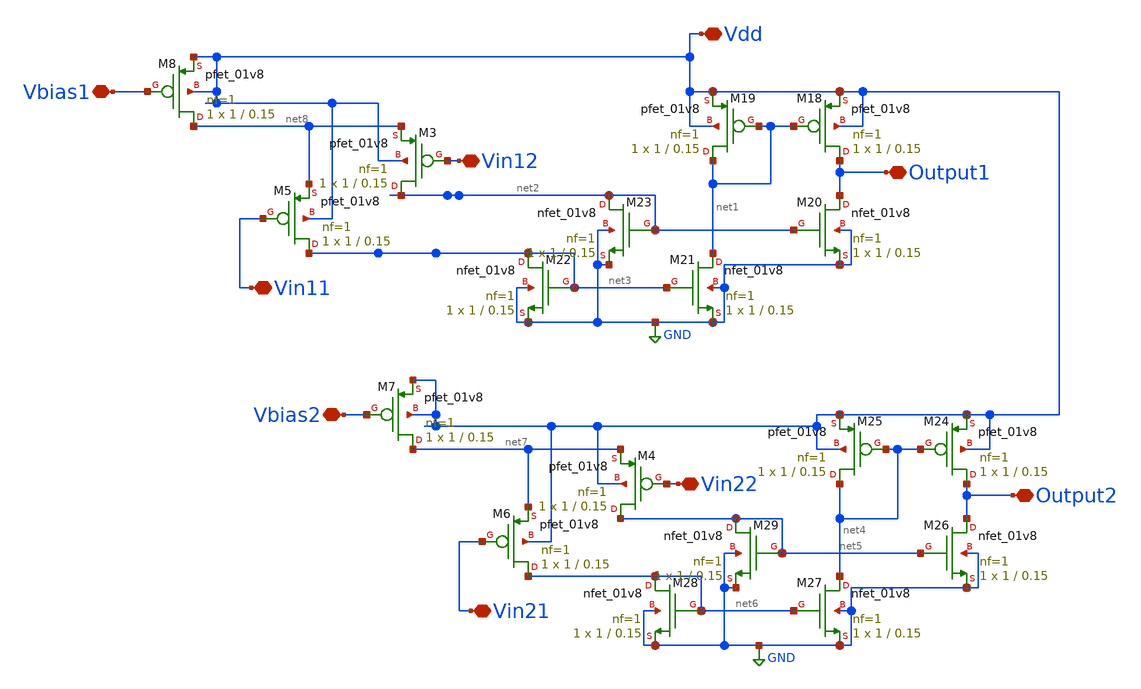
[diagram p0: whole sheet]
** sch_path: libs.ref/sky130_hilas_sc/xschem/TA2SignalBiasCell.sch
**.subckt TA2SignalBiasCell Vdd Output1 Output2 Vin21 Vin22 Vin11 Vin12 Vbias1 Vbias2
*.iopin Vdd
*.iopin Output1
*.iopin Output2
*.iopin Vin21
*.iopin Vin22
*.iopin Vin11
*.iopin Vin12
*.iopin Vbias1
*.iopin Vbias2
XM18 Output1 net1 Vdd Vdd sky130_fd_pr__pfet_01v8 L=0.15 W=1 nf=1 ad='int((nf+1)/2) * W/nf * 0.29' as='int((nf+2)/2) * W/nf * 0.29'
+ pd='2*int((nf+1)/2) * (W/nf + 0.29)' ps='2*int((nf+2)/2) * (W/nf + 0.29)' nrd='0.29 / W' nrs='0.29 / W'
+ sa=0 sb=0 sd=0 mult=1 m=1
XM19 net1 net1 Vdd Vdd sky130_fd_pr__pfet_01v8 L=0.15 W=1 nf=1 ad='int((nf+1)/2) * W/nf * 0.29' as='int((nf+2)/2) * W/nf * 0.29'
+ pd='2*int((nf+1)/2) * (W/nf + 0.29)' ps='2*int((nf+2)/2) * (W/nf + 0.29)' nrd='0.29 / W' nrs='0.29 / W'
+ sa=0 sb=0 sd=0 mult=1 m=1
XM20 Output1 net2 GND GND sky130_fd_pr__nfet_01v8 L=0.15 W=1 nf=1 ad='int((nf+1)/2) * W/nf * 0.29' as='int((nf+2)/2) * W/nf * 0.29'
+ pd='2*int((nf+1)/2) * (W/nf + 0.29)' ps='2*int((nf+2)/2) * (W/nf + 0.29)' nrd='0.29 / W' nrs='0.29 / W'
+ sa=0 sb=0 sd=0 mult=1 m=1
XM21 net1 net3 GND GND sky130_fd_pr__nfet_01v8 L=0.15 W=1 nf=1 ad='int((nf+1)/2) * W/nf * 0.29' as='int((nf+2)/2) * W/nf * 0.29'
+ pd='2*int((nf+1)/2) * (W/nf + 0.29)' ps='2*int((nf+2)/2) * (W/nf + 0.29)' nrd='0.29 / W' nrs='0.29 / W'
+ sa=0 sb=0 sd=0 mult=1 m=1
XM22 net3 net3 GND GND sky130_fd_pr__nfet_01v8 L=0.15 W=1 nf=1 ad='int((nf+1)/2) * W/nf * 0.29' as='int((nf+2)/2) * W/nf * 0.29'
+ pd='2*int((nf+1)/2) * (W/nf + 0.29)' ps='2*int((nf+2)/2) * (W/nf + 0.29)' nrd='0.29 / W' nrs='0.29 / W'
+ sa=0 sb=0 sd=0 mult=1 m=1
XM23 net2 net2 GND GND sky130_fd_pr__nfet_01v8 L=0.15 W=1 nf=1 ad='int((nf+1)/2) * W/nf * 0.29' as='int((nf+2)/2) * W/nf * 0.29'
+ pd='2*int((nf+1)/2) * (W/nf + 0.29)' ps='2*int((nf+2)/2) * (W/nf + 0.29)' nrd='0.29 / W' nrs='0.29 / W'
+ sa=0 sb=0 sd=0 mult=1 m=1
XM24 Output2 net4 Vdd Vdd sky130_fd_pr__pfet_01v8 L=0.15 W=1 nf=1 ad='int((nf+1)/2) * W/nf * 0.29' as='int((nf+2)/2) * W/nf * 0.29'
+ pd='2*int((nf+1)/2) * (W/nf + 0.29)' ps='2*int((nf+2)/2) * (W/nf + 0.29)' nrd='0.29 / W' nrs='0.29 / W'
+ sa=0 sb=0 sd=0 mult=1 m=1
XM25 net4 net4 Vdd Vdd sky130_fd_pr__pfet_01v8 L=0.15 W=1 nf=1 ad='int((nf+1)/2) * W/nf * 0.29' as='int((nf+2)/2) * W/nf * 0.29'
+ pd='2*int((nf+1)/2) * (W/nf + 0.29)' ps='2*int((nf+2)/2) * (W/nf + 0.29)' nrd='0.29 / W' nrs='0.29 / W'
+ sa=0 sb=0 sd=0 mult=1 m=1
XM26 Output2 net5 GND GND sky130_fd_pr__nfet_01v8 L=0.15 W=1 nf=1 ad='int((nf+1)/2) * W/nf * 0.29' as='int((nf+2)/2) * W/nf * 0.29'
+ pd='2*int((nf+1)/2) * (W/nf + 0.29)' ps='2*int((nf+2)/2) * (W/nf + 0.29)' nrd='0.29 / W' nrs='0.29 / W'
+ sa=0 sb=0 sd=0 mult=1 m=1
XM27 net4 net6 GND GND sky130_fd_pr__nfet_01v8 L=0.15 W=1 nf=1 ad='int((nf+1)/2) * W/nf * 0.29' as='int((nf+2)/2) * W/nf * 0.29'
+ pd='2*int((nf+1)/2) * (W/nf + 0.29)' ps='2*int((nf+2)/2) * (W/nf + 0.29)' nrd='0.29 / W' nrs='0.29 / W'
+ sa=0 sb=0 sd=0 mult=1 m=1
XM28 net6 net6 GND GND sky130_fd_pr__nfet_01v8 L=0.15 W=1 nf=1 ad='int((nf+1)/2) * W/nf * 0.29' as='int((nf+2)/2) * W/nf * 0.29'
+ pd='2*int((nf+1)/2) * (W/nf + 0.29)' ps='2*int((nf+2)/2) * (W/nf + 0.29)' nrd='0.29 / W' nrs='0.29 / W'
+ sa=0 sb=0 sd=0 mult=1 m=1
XM29 net5 net5 GND GND sky130_fd_pr__nfet_01v8 L=0.15 W=1 nf=1 ad='int((nf+1)/2) * W/nf * 0.29' as='int((nf+2)/2) * W/nf * 0.29'
+ pd='2*int((nf+1)/2) * (W/nf + 0.29)' ps='2*int((nf+2)/2) * (W/nf + 0.29)' nrd='0.29 / W' nrs='0.29 / W'
+ sa=0 sb=0 sd=0 mult=1 m=1
XM3 net2 Vin12 net8 Vdd sky130_fd_pr__pfet_01v8 L=0.15 W=1 nf=1 ad='int((nf+1)/2) * W/nf * 0.29' as='int((nf+2)/2) * W/nf * 0.29'
+ pd='2*int((nf+1)/2) * (W/nf + 0.29)' ps='2*int((nf+2)/2) * (W/nf + 0.29)' nrd='0.29 / W' nrs='0.29 / W'
+ sa=0 sb=0 sd=0 mult=1 m=1
XM4 net5 Vin22 net7 Vdd sky130_fd_pr__pfet_01v8 L=0.15 W=1 nf=1 ad='int((nf+1)/2) * W/nf * 0.29' as='int((nf+2)/2) * W/nf * 0.29'
+ pd='2*int((nf+1)/2) * (W/nf + 0.29)' ps='2*int((nf+2)/2) * (W/nf + 0.29)' nrd='0.29 / W' nrs='0.29 / W'
+ sa=0 sb=0 sd=0 mult=1 m=1
XM5 net3 Vin11 net8 Vdd sky130_fd_pr__pfet_01v8 L=0.15 W=1 nf=1 ad='int((nf+1)/2) * W/nf * 0.29' as='int((nf+2)/2) * W/nf * 0.29'
+ pd='2*int((nf+1)/2) * (W/nf + 0.29)' ps='2*int((nf+2)/2) * (W/nf + 0.29)' nrd='0.29 / W' nrs='0.29 / W'
+ sa=0 sb=0 sd=0 mult=1 m=1
XM6 net6 Vin21 net7 Vdd sky130_fd_pr__pfet_01v8 L=0.15 W=1 nf=1 ad='int((nf+1)/2) * W/nf * 0.29' as='int((nf+2)/2) * W/nf * 0.29'
+ pd='2*int((nf+1)/2) * (W/nf + 0.29)' ps='2*int((nf+2)/2) * (W/nf + 0.29)' nrd='0.29 / W' nrs='0.29 / W'
+ sa=0 sb=0 sd=0 mult=1 m=1
XM7 net7 Vbias2 Vdd Vdd sky130_fd_pr__pfet_01v8 L=0.15 W=1 nf=1 ad='int((nf+1)/2) * W/nf * 0.29' as='int((nf+2)/2) * W/nf * 0.29'
+ pd='2*int((nf+1)/2) * (W/nf + 0.29)' ps='2*int((nf+2)/2) * (W/nf + 0.29)' nrd='0.29 / W' nrs='0.29 / W'
+ sa=0 sb=0 sd=0 mult=1 m=1
XM8 net8 Vbias1 Vdd Vdd sky130_fd_pr__pfet_01v8 L=0.15 W=1 nf=1 ad='int((nf+1)/2) * W/nf * 0.29' as='int((nf+2)/2) * W/nf * 0.29'
+ pd='2*int((nf+1)/2) * (W/nf + 0.29)' ps='2*int((nf+2)/2) * (W/nf + 0.29)' nrd='0.29 / W' nrs='0.29 / W'
+ sa=0 sb=0 sd=0 mult=1 m=1
**.ends
.GLOBAL GND
.end
